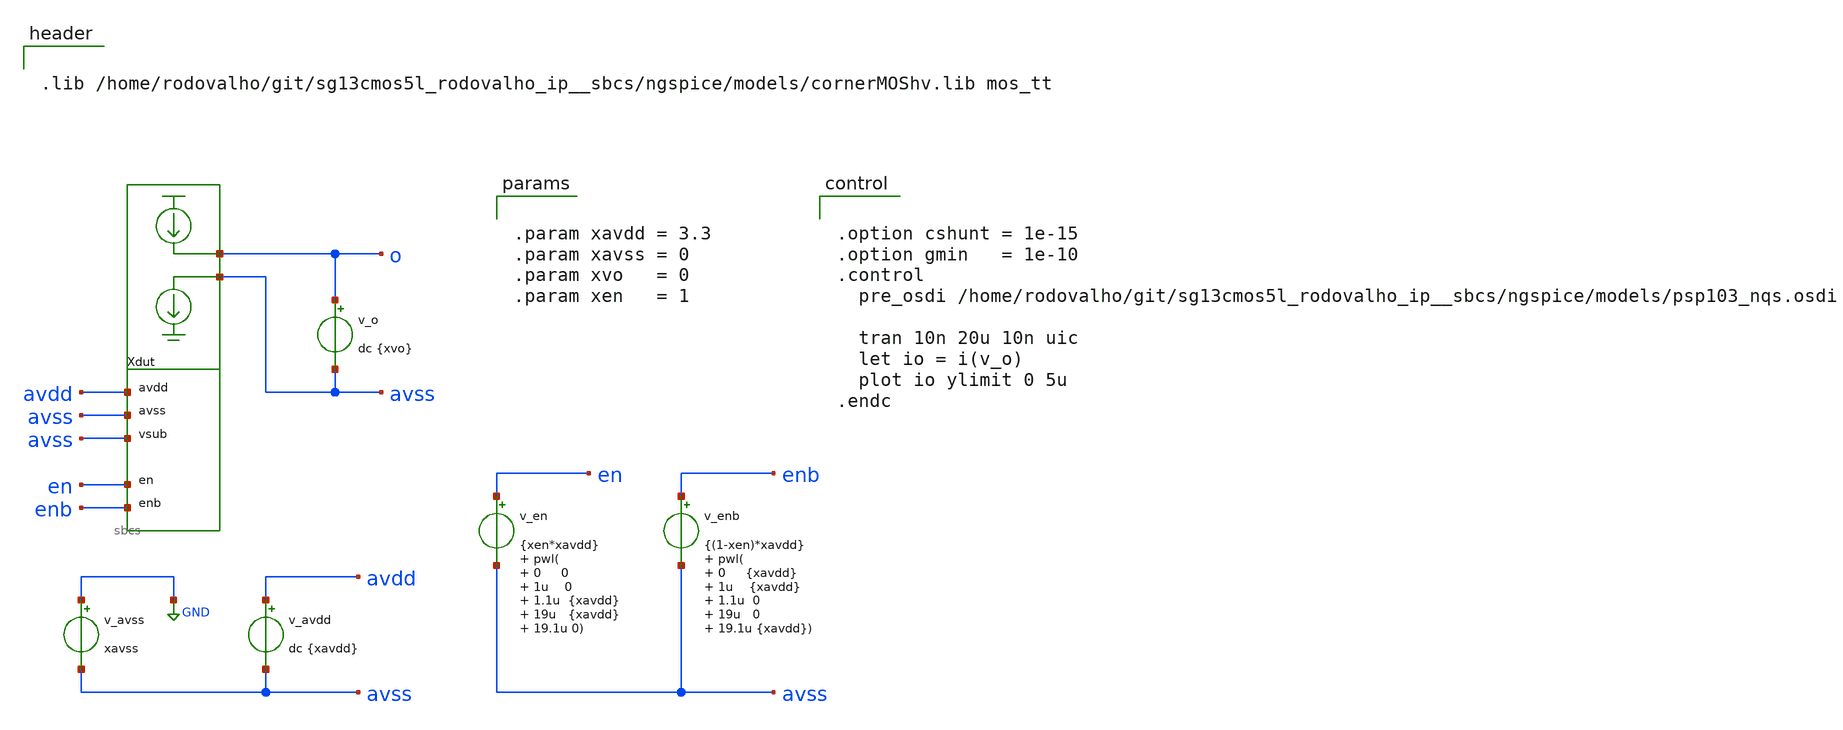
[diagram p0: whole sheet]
** sch_path: xschem/tb_sbcs_tran.sch
**.subckt tb_sbcs_tran
Xdut o avss avdd avss en enb sbcs
v_avss GND avss xavss
v_avdd avdd avss dc {xavdd}
v_en en avss {xen*xavdd} pwl( 0 0 1u 0 1.1u {xavdd} 19u {xavdd} 19.1u 0)
v_enb enb avss {(1-xen)*xavdd} pwl( 0 {xavdd} 1u {xavdd} 1.1u 0 19u 0 19.1u {xavdd})

v_o o avss dc {xvo}
**** begin user architecture code


.lib /home/rodovalho/git/sg13cmos5l_rodovalho_ip__sbcs/ngspice/models/cornerMOShv.lib mos_tt




.option cshunt = 1e-15
.option gmin   = 1e-10
.control
  pre_osdi /home/rodovalho/git/sg13cmos5l_rodovalho_ip__sbcs/ngspice/models/psp103_nqs.osdi

  tran 10n 20u 10n uic
  let io = i(v_o)
  plot io ylimit 0 5u
.endc




.param xavdd = 3.3
.param xavss = 0
.param xvo   = 0
.param xen   = 1


**** end user architecture code
**.ends
.GLOBAL GND
.end
